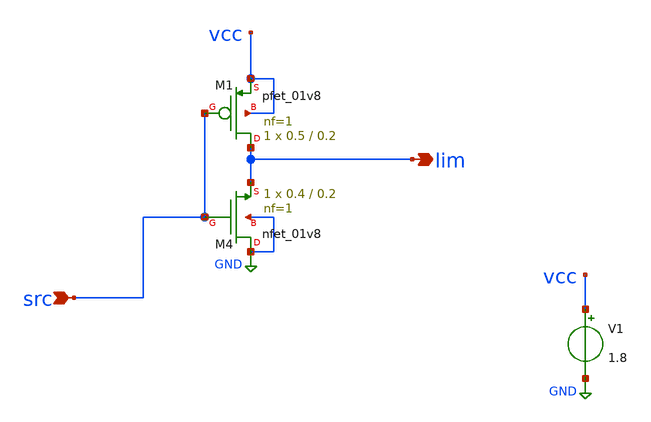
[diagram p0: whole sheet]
** sch_path: xschem/dlim.sch
**.subckt dlim src lim
*.ipin src
*.opin lim
XM4 GND src lim GND sky130_fd_pr__nfet_01v8 L=0.2 W=0.4 nf=1 ad='int((nf+1)/2) * W/nf * 0.29' as='int((nf+2)/2) * W/nf * 0.29'
+ pd='2*int((nf+1)/2) * (W/nf + 0.29)' ps='2*int((nf+2)/2) * (W/nf + 0.29)' nrd='0.29 / W' nrs='0.29 / W'
+ sa=0 sb=0 sd=0 mult=1 m=1
V1 vcc GND 1.8
XM1 lim src vcc vcc sky130_fd_pr__pfet_01v8 L=0.2 W=0.5 nf=1 ad='int((nf+1)/2) * W/nf * 0.29' as='int((nf+2)/2) * W/nf * 0.29'
+ pd='2*int((nf+1)/2) * (W/nf + 0.29)' ps='2*int((nf+2)/2) * (W/nf + 0.29)' nrd='0.29 / W' nrs='0.29 / W'
+ sa=0 sb=0 sd=0 mult=1 m=1
**.ends
.GLOBAL GND
.end
